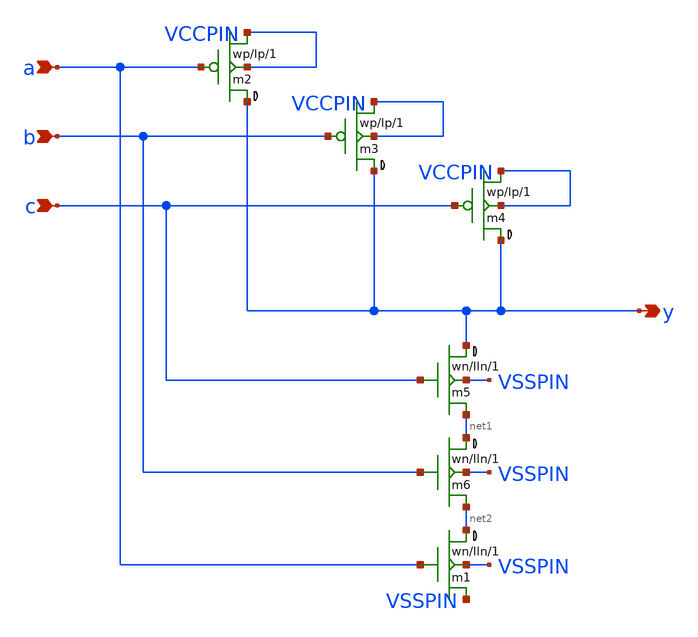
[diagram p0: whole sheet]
** sch_path: xschem_libs_newsym/rom8k/lvnand3/schematic/lvnand3.sch
* Copyright (C) 1998-2024 Stefan Frederik Schippers
* This program is free software; you can redistribute it and/or modify
* it under the terms of the GNU General Public License as published by
* the Free Software Foundation; either version 2 of the License, or
* (at your option) any later version.
* This program is distributed in the hope that it will be useful,
* but WITHOUT ANY WARRANTY; without even the implied warranty of
* MERCHANTABILITY or FITNESS FOR A PARTICULAR PURPOSE.  See the
* GNU General Public License for more details.
* You should have received a copy of the GNU General Public License
* along with this program; if not, write to the Free Software
**.subckt lvnand3 y a b c
*.opin y
*.ipin a
*.ipin b
*.ipin c
m1 net2 a VSSPIN VSSPIN cmosn w=wn l=lln ad={wn *2.2u} as={wn *2.2u} pd={wn *2+4.4u} ps={wn *2+4.4u}
+ m=1
m2 y a VCCPIN VCCPIN cmosp w=wp l=lp ad={wp *2.2u} as={wp *2.2u} pd={wp *2+4.4u} ps={wp *2+4.4u} m=1
m3 y b VCCPIN VCCPIN cmosp w=wp l=lp ad={wp *2.2u} as={wp *2.2u} pd={wp *2+4.4u} ps={wp *2+4.4u} m=1
m5 y c net1 VSSPIN cmosn w=wn l=lln ad={wn *2.2u} as={wn *2.2u} pd={wn *2+4.4u} ps={wn *2+4.4u} m=1
m4 y c VCCPIN VCCPIN cmosp w=wp l=lp ad={wp *2.2u} as={wp *2.2u} pd={wp *2+4.4u} ps={wp *2+4.4u} m=1
m6 net1 b net2 VSSPIN cmosn w=wn l=lln ad={wn *2.2u} as={wn *2.2u} pd={wn *2+4.4u} ps={wn *2+4.4u} m=1
**.ends
.end
